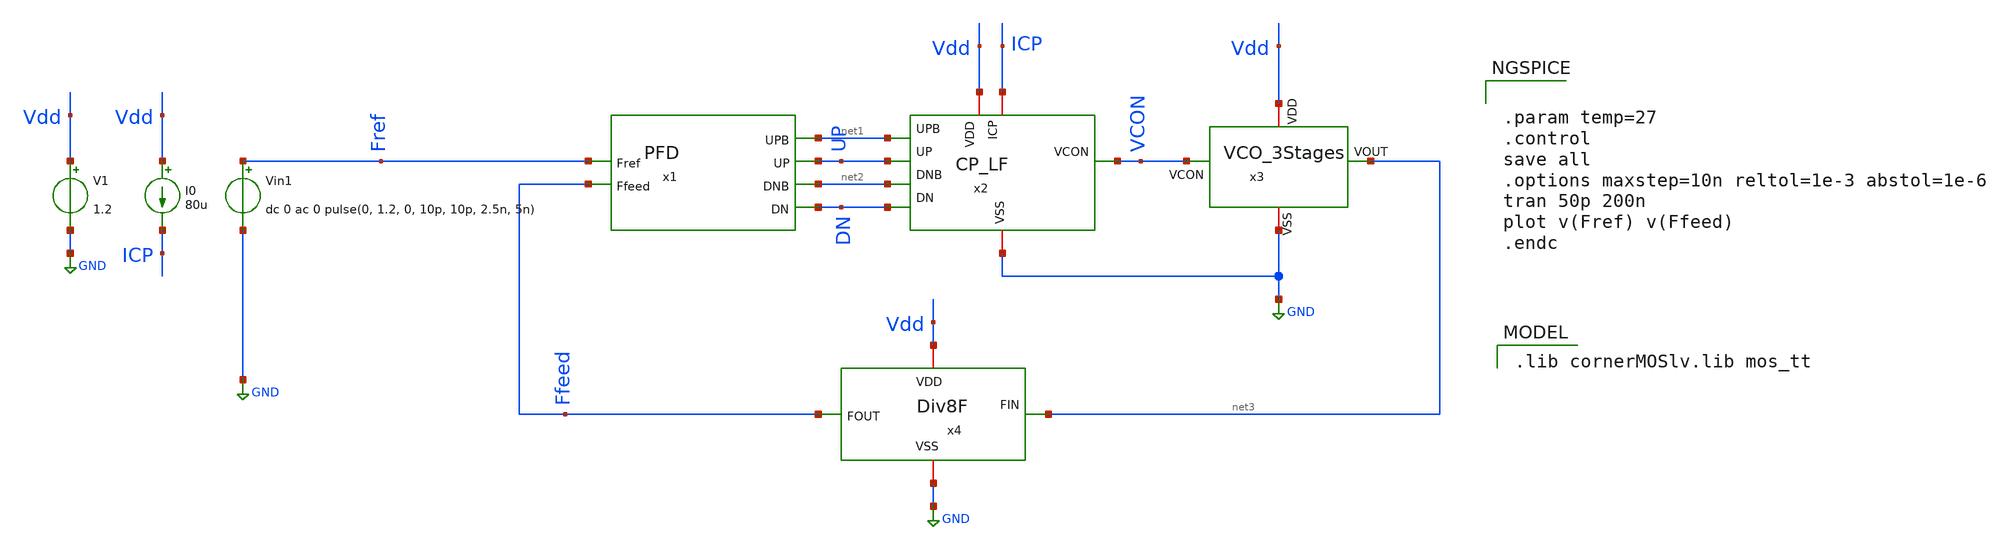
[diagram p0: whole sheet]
** sch_path: Team 1 Design/design_data/xschem/PLL_Completed/PLL_Completed_tb.sch
**.subckt PLL_Completed_tb
x1 Fref UP net1 DN net2 Ffeed PFD
x2 Vdd ICP GND net1 UP VCON net2 DN CP_LF
x3 Vdd net3 VCON GND VCO_3Stages
x4 Vdd Ffeed net3 GND Div8F
V1 Vdd GND 1.2
I0 Vdd ICP 80u
Vin1 Fref GND dc 0 ac 0 pulse(0, 1.2, 0, 10p, 10p, 2.5n, 5n)
**** begin user architecture code


.param temp=27
.control
save all
.options maxstep=10n reltol=1e-3 abstol=1e-6
tran 50p 200n
plot v(Fref) v(Ffeed)
.endc


 .lib cornerMOSlv.lib mos_tt

**** end user architecture code
**.ends
.GLOBAL GND
.end
